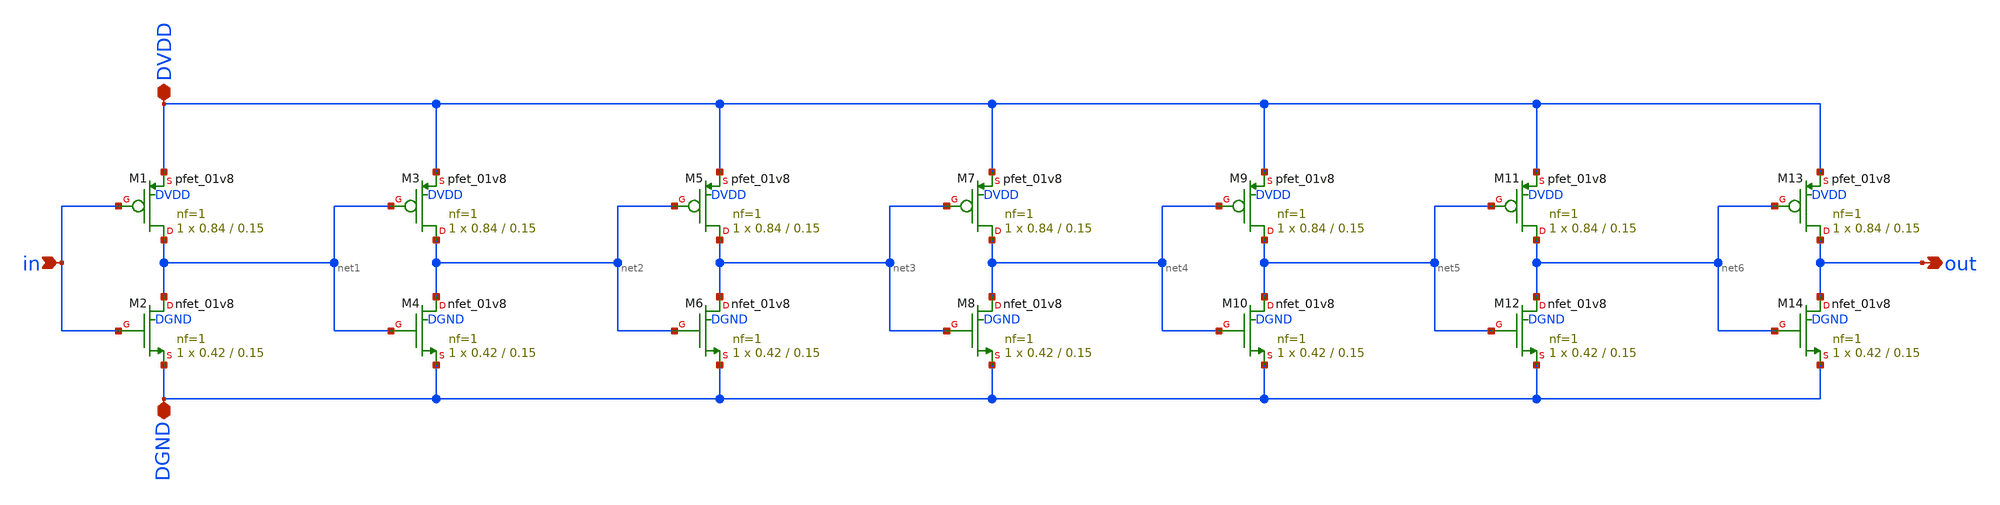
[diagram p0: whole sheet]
** sch_path: tutorial-4/source/q2/osc.sch
**.subckt osc in DVDD DGND out
*.ipin in
*.iopin DVDD
*.iopin DGND
*.opin out
XM1 net1 in DVDD DVDD sky130_fd_pr__pfet_01v8 L=0.15 W=0.84 nf=1 ad='int((nf+1)/2) * W/nf * 0.29' as='int((nf+2)/2) * W/nf * 0.29'
+ pd='2*int((nf+1)/2) * (W/nf + 0.29)' ps='2*int((nf+2)/2) * (W/nf + 0.29)' nrd='0.29 / W' nrs='0.29 / W'
+ sa=0 sb=0 sd=0 mult=1 m=1
XM2 net1 in DGND DGND sky130_fd_pr__nfet_01v8 L=0.15 W=0.42 nf=1 ad='int((nf+1)/2) * W/nf * 0.29' as='int((nf+2)/2) * W/nf * 0.29'
+ pd='2*int((nf+1)/2) * (W/nf + 0.29)' ps='2*int((nf+2)/2) * (W/nf + 0.29)' nrd='0.29 / W' nrs='0.29 / W'
+ sa=0 sb=0 sd=0 mult=1 m=1
XM3 net2 net1 DVDD DVDD sky130_fd_pr__pfet_01v8 L=0.15 W=0.84 nf=1 ad='int((nf+1)/2) * W/nf * 0.29' as='int((nf+2)/2) * W/nf * 0.29'
+ pd='2*int((nf+1)/2) * (W/nf + 0.29)' ps='2*int((nf+2)/2) * (W/nf + 0.29)' nrd='0.29 / W' nrs='0.29 / W'
+ sa=0 sb=0 sd=0 mult=1 m=1
XM4 net2 net1 DGND DGND sky130_fd_pr__nfet_01v8 L=0.15 W=0.42 nf=1 ad='int((nf+1)/2) * W/nf * 0.29' as='int((nf+2)/2) * W/nf * 0.29'
+ pd='2*int((nf+1)/2) * (W/nf + 0.29)' ps='2*int((nf+2)/2) * (W/nf + 0.29)' nrd='0.29 / W' nrs='0.29 / W'
+ sa=0 sb=0 sd=0 mult=1 m=1
XM5 net3 net2 DVDD DVDD sky130_fd_pr__pfet_01v8 L=0.15 W=0.84 nf=1 ad='int((nf+1)/2) * W/nf * 0.29' as='int((nf+2)/2) * W/nf * 0.29'
+ pd='2*int((nf+1)/2) * (W/nf + 0.29)' ps='2*int((nf+2)/2) * (W/nf + 0.29)' nrd='0.29 / W' nrs='0.29 / W'
+ sa=0 sb=0 sd=0 mult=1 m=1
XM6 net3 net2 DGND DGND sky130_fd_pr__nfet_01v8 L=0.15 W=0.42 nf=1 ad='int((nf+1)/2) * W/nf * 0.29' as='int((nf+2)/2) * W/nf * 0.29'
+ pd='2*int((nf+1)/2) * (W/nf + 0.29)' ps='2*int((nf+2)/2) * (W/nf + 0.29)' nrd='0.29 / W' nrs='0.29 / W'
+ sa=0 sb=0 sd=0 mult=1 m=1
XM7 net4 net3 DVDD DVDD sky130_fd_pr__pfet_01v8 L=0.15 W=0.84 nf=1 ad='int((nf+1)/2) * W/nf * 0.29' as='int((nf+2)/2) * W/nf * 0.29'
+ pd='2*int((nf+1)/2) * (W/nf + 0.29)' ps='2*int((nf+2)/2) * (W/nf + 0.29)' nrd='0.29 / W' nrs='0.29 / W'
+ sa=0 sb=0 sd=0 mult=1 m=1
XM8 net4 net3 DGND DGND sky130_fd_pr__nfet_01v8 L=0.15 W=0.42 nf=1 ad='int((nf+1)/2) * W/nf * 0.29' as='int((nf+2)/2) * W/nf * 0.29'
+ pd='2*int((nf+1)/2) * (W/nf + 0.29)' ps='2*int((nf+2)/2) * (W/nf + 0.29)' nrd='0.29 / W' nrs='0.29 / W'
+ sa=0 sb=0 sd=0 mult=1 m=1
XM9 net5 net4 DVDD DVDD sky130_fd_pr__pfet_01v8 L=0.15 W=0.84 nf=1 ad='int((nf+1)/2) * W/nf * 0.29' as='int((nf+2)/2) * W/nf * 0.29'
+ pd='2*int((nf+1)/2) * (W/nf + 0.29)' ps='2*int((nf+2)/2) * (W/nf + 0.29)' nrd='0.29 / W' nrs='0.29 / W'
+ sa=0 sb=0 sd=0 mult=1 m=1
XM10 net5 net4 DGND DGND sky130_fd_pr__nfet_01v8 L=0.15 W=0.42 nf=1 ad='int((nf+1)/2) * W/nf * 0.29'
+ as='int((nf+2)/2) * W/nf * 0.29' pd='2*int((nf+1)/2) * (W/nf + 0.29)' ps='2*int((nf+2)/2) * (W/nf + 0.29)'
+ nrd='0.29 / W' nrs='0.29 / W' sa=0 sb=0 sd=0 mult=1 m=1
XM11 net6 net5 DVDD DVDD sky130_fd_pr__pfet_01v8 L=0.15 W=0.84 nf=1 ad='int((nf+1)/2) * W/nf * 0.29'
+ as='int((nf+2)/2) * W/nf * 0.29' pd='2*int((nf+1)/2) * (W/nf + 0.29)' ps='2*int((nf+2)/2) * (W/nf + 0.29)'
+ nrd='0.29 / W' nrs='0.29 / W' sa=0 sb=0 sd=0 mult=1 m=1
XM12 net6 net5 DGND DGND sky130_fd_pr__nfet_01v8 L=0.15 W=0.42 nf=1 ad='int((nf+1)/2) * W/nf * 0.29'
+ as='int((nf+2)/2) * W/nf * 0.29' pd='2*int((nf+1)/2) * (W/nf + 0.29)' ps='2*int((nf+2)/2) * (W/nf + 0.29)'
+ nrd='0.29 / W' nrs='0.29 / W' sa=0 sb=0 sd=0 mult=1 m=1
XM13 out net6 DVDD DVDD sky130_fd_pr__pfet_01v8 L=0.15 W=0.84 nf=1 ad='int((nf+1)/2) * W/nf * 0.29' as='int((nf+2)/2) * W/nf * 0.29'
+ pd='2*int((nf+1)/2) * (W/nf + 0.29)' ps='2*int((nf+2)/2) * (W/nf + 0.29)' nrd='0.29 / W' nrs='0.29 / W'
+ sa=0 sb=0 sd=0 mult=1 m=1
XM14 out net6 DGND DGND sky130_fd_pr__nfet_01v8 L=0.15 W=0.42 nf=1 ad='int((nf+1)/2) * W/nf * 0.29' as='int((nf+2)/2) * W/nf * 0.29'
+ pd='2*int((nf+1)/2) * (W/nf + 0.29)' ps='2*int((nf+2)/2) * (W/nf + 0.29)' nrd='0.29 / W' nrs='0.29 / W'
+ sa=0 sb=0 sd=0 mult=1 m=1
**.ends
.end
